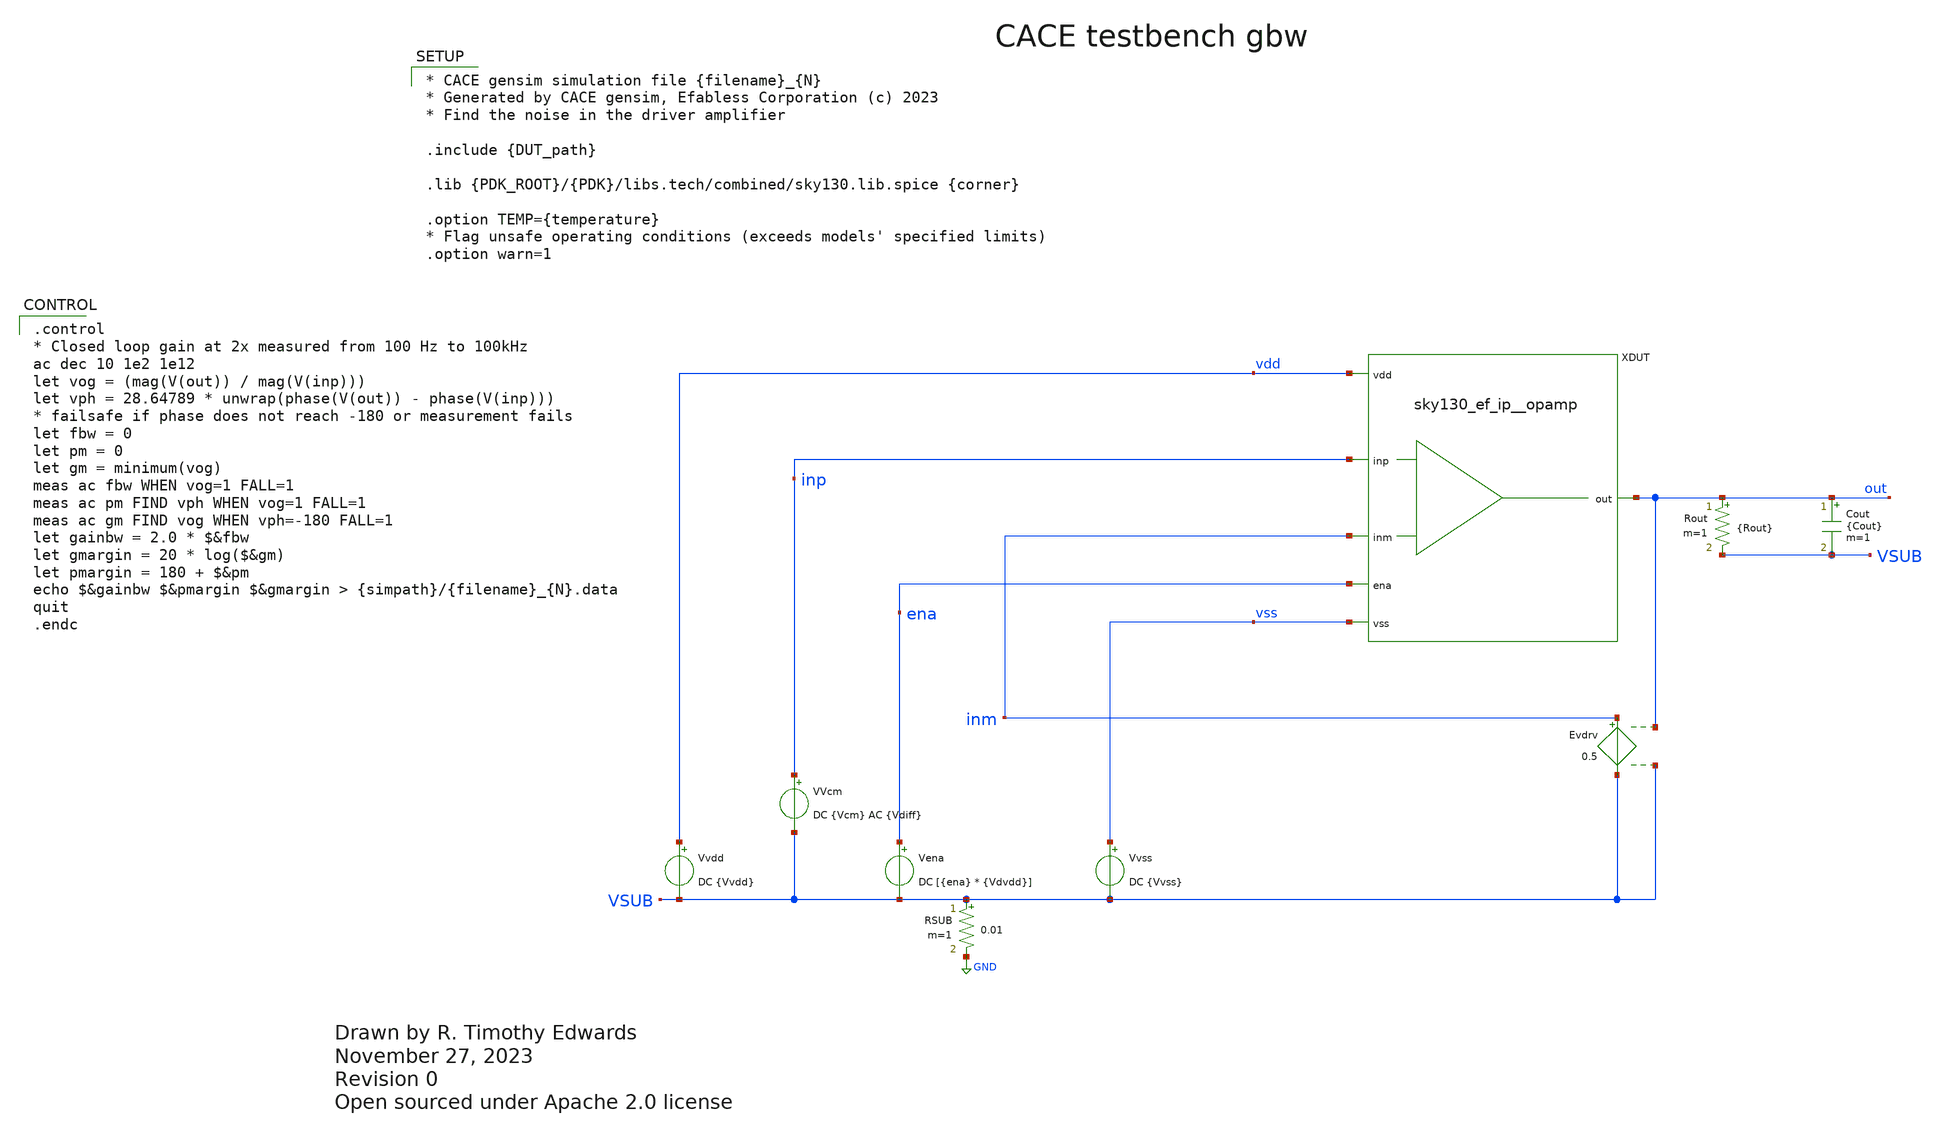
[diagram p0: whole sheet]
** sch_path: cace/templates/gbw.sch
* Open sourced under Apache 2.0 license
**.subckt gbw
VVcm inp VSUB DC {Vcm} AC {Vdiff}
Vena ena VSUB DC [{ena} * {Vdvdd}]
Vvss vss VSUB DC {Vvss}
Rout out VSUB {Rout} m=1
Cout out VSUB {Cout} m=1
Vvdd vdd VSUB DC {Vvdd}
RSUB VSUB GND 0.01 m=1
XDUT vdd out ena vss inp inm sky130_ef_ip__opamp
Evdrv inm VSUB out VSUB 0.5
**** begin user architecture code

.control
* Closed loop gain at 2x measured from 100 Hz to 100kHz
ac dec 10 1e2 1e12
let vog = (mag(V(out)) / mag(V(inp)))
let vph = 28.64789 * unwrap(phase(V(out)) - phase(V(inp)))
* failsafe if phase does not reach -180 or measurement fails
let fbw = 0
let pm = 0
let gm = minimum(vog)
meas ac fbw WHEN vog=1 FALL=1
meas ac pm FIND vph WHEN vog=1 FALL=1
meas ac gm FIND vog WHEN vph=-180 FALL=1
let gainbw = 2.0 * $&fbw
let gmargin = 20 * log($&gm)
let pmargin = 180 + $&pm
echo $&gainbw $&pmargin $&gmargin > {simpath}/{filename}_{N}.data
quit
.endc



* CACE gensim simulation file {filename}_{N}
* Generated by CACE gensim, Efabless Corporation (c) 2023
* Find the noise in the driver amplifier

.include {DUT_path}

.lib {PDK_ROOT}/{PDK}/libs.tech/combined/sky130.lib.spice {corner}

.option TEMP={temperature}
* Flag unsafe operating conditions (exceeds models' specified limits)
.option warn=1


**** end user architecture code
**.ends

* expanding   symbol:  sky130_ef_ip__opamp.sym # of pins=6
** sym_path: xschem/sky130_ef_ip__opamp.sym
** sch_path: xschem/sky130_ef_ip__opamp.sch
.subckt sky130_ef_ip__opamp vdd out ena vss inp inm
*.ipin inp
*.ipin vdd
*.ipin vss
*.opin out
*.ipin ena
*.ipin inm
XM4 pdrv1 net1 vdd vdd sky130_fd_pr__pfet_g5v0d10v5 L=0.5 W=2 nf=2 ad='int((nf+1)/2) * W/nf * 0.29' as='int((nf+2)/2)
+ * W/nf * 0.29' pd='2*int((nf+1)/2) * (W/nf + 0.29)' ps='2*int((nf+2)/2) * (W/nf + 0.29)' nrd='0.29 /
+ W' nrs='0.29 / W' sa=0 sb=0 sd=0 mult=1 m=1
XM5 vdd net1 net1 vdd sky130_fd_pr__pfet_g5v0d10v5 L=0.5 W=2 nf=2 ad='int((nf+1)/2) * W/nf * 0.29' as='int((nf+2)/2)
+ * W/nf * 0.29' pd='2*int((nf+1)/2) * (W/nf + 0.29)' ps='2*int((nf+2)/2) * (W/nf + 0.29)' nrd='0.29 /
+ W' nrs='0.29 / W' sa=0 sb=0 sd=0 mult=1 m=1
XM9 vcomn1 nbias vss vss sky130_fd_pr__nfet_g5v0d10v5 L=0.5 W=1 nf=1 ad='int((nf+1)/2) * W/nf * 0.29' as='int((nf+2)/2)
+ * W/nf * 0.29' pd='2*int((nf+1)/2) * (W/nf + 0.29)' ps='2*int((nf+2)/2) * (W/nf + 0.29)' nrd='0.29 /
+ W' nrs='0.29 / W' sa=0 sb=0 sd=0 mult=1 m=1
XM10 vss nbias nbias vss sky130_fd_pr__nfet_g5v0d10v5 L=0.5 W=4 nf=4 ad='int((nf+1)/2) * W/nf * 0.29' as='int((nf+2)/2)
+ * W/nf * 0.29' pd='2*int((nf+1)/2) * (W/nf + 0.29)' ps='2*int((nf+2)/2) * (W/nf + 0.29)' nrd='0.29 /
+ W' nrs='0.29 / W' sa=0 sb=0 sd=0 mult=1 m=1
XR1 net4 vdd vss sky130_fd_pr__res_xhigh_po_0p35 W=1 L=100 mult=1 m=1
XM20 out pdrv1 vdd vdd sky130_fd_pr__pfet_g5v0d10v5 L=0.5 W=200 nf=200 ad='int((nf+1)/2) * W/nf * 0.29' as='int((nf+2)/2)
+ * W/nf * 0.29' pd='2*int((nf+1)/2) * (W/nf + 0.29)' ps='2*int((nf+2)/2) * (W/nf + 0.29)' nrd='0.29 /
+ W' nrs='0.29 / W' sa=0 sb=0 sd=0 mult=1 m=1
XM22 out ndrv vss vss sky130_fd_pr__nfet_g5v0d10v5 L=0.5 W=120 nf=120 ad='int((nf+1)/2) * W/nf * 0.29' as='int((nf+2)/2)
+ * W/nf * 0.29' pd='2*int((nf+1)/2) * (W/nf + 0.29)' ps='2*int((nf+2)/2) * (W/nf + 0.29)' nrd='0.29 /
+ W' nrs='0.29 / W' sa=0 sb=0 sd=0 mult=1 m=1
XM24 pbias nbias vss vss sky130_fd_pr__nfet_g5v0d10v5 L=0.5 W=1 nf=1 ad='int((nf+1)/2) * W/nf * 0.29' as='int((nf+2)/2)
+ * W/nf * 0.29' pd='2*int((nf+1)/2) * (W/nf + 0.29)' ps='2*int((nf+2)/2) * (W/nf + 0.29)' nrd='0.29 /
+ W' nrs='0.29 / W' sa=0 sb=0 sd=0 mult=1 m=1
XM25 vdd pbias pbias vdd sky130_fd_pr__pfet_g5v0d10v5 L=0.5 W=1 nf=1 ad='int((nf+1)/2) * W/nf * 0.29' as='int((nf+2)/2)
+ * W/nf * 0.29' pd='2*int((nf+1)/2) * (W/nf + 0.29)' ps='2*int((nf+2)/2) * (W/nf + 0.29)' nrd='0.29 /
+ W' nrs='0.29 / W' sa=0 sb=0 sd=0 mult=1 m=1
XM26 vcomp pbias vdd vdd sky130_fd_pr__pfet_g5v0d10v5 L=0.5 W=2 nf=2 ad='int((nf+1)/2) * W/nf * 0.29' as='int((nf+2)/2)
+ * W/nf * 0.29' pd='2*int((nf+1)/2) * (W/nf + 0.29)' ps='2*int((nf+2)/2) * (W/nf + 0.29)' nrd='0.29 /
+ W' nrs='0.29 / W' sa=0 sb=0 sd=0 mult=1 m=1
XM27 net2 inm vcomp vdd sky130_fd_pr__pfet_g5v0d10v5 L=0.5 W=2 nf=2 ad='int((nf+1)/2) * W/nf * 0.29' as='int((nf+2)/2)
+ * W/nf * 0.29' pd='2*int((nf+1)/2) * (W/nf + 0.29)' ps='2*int((nf+2)/2) * (W/nf + 0.29)' nrd='0.29 /
+ W' nrs='0.29 / W' sa=0 sb=0 sd=0 mult=1 m=1
XM28 vcomp inp ndrv vdd sky130_fd_pr__pfet_g5v0d10v5 L=0.5 W=2 nf=2 ad='int((nf+1)/2) * W/nf * 0.29' as='int((nf+2)/2)
+ * W/nf * 0.29' pd='2*int((nf+1)/2) * (W/nf + 0.29)' ps='2*int((nf+2)/2) * (W/nf + 0.29)' nrd='0.29 /
+ W' nrs='0.29 / W' sa=0 sb=0 sd=0 mult=1 m=1
XM29 ndrv net2 vss vss sky130_fd_pr__nfet_g5v0d10v5 L=0.5 W=1 nf=1 ad='int((nf+1)/2) * W/nf * 0.29' as='int((nf+2)/2)
+ * W/nf * 0.29' pd='2*int((nf+1)/2) * (W/nf + 0.29)' ps='2*int((nf+2)/2) * (W/nf + 0.29)' nrd='0.29 /
+ W' nrs='0.29 / W' sa=0 sb=0 sd=0 mult=1 m=1
XM30 vss net2 net2 vss sky130_fd_pr__nfet_g5v0d10v5 L=0.5 W=1 nf=1 ad='int((nf+1)/2) * W/nf * 0.29' as='int((nf+2)/2)
+ * W/nf * 0.29' pd='2*int((nf+1)/2) * (W/nf + 0.29)' ps='2*int((nf+2)/2) * (W/nf + 0.29)' nrd='0.29 /
+ W' nrs='0.29 / W' sa=0 sb=0 sd=0 mult=1 m=1
XM1 net1 inm vcomn1 vss sky130_fd_pr__nfet_g5v0d10v5 L=0.5 W=1 nf=1 ad='int((nf+1)/2) * W/nf * 0.29' as='int((nf+2)/2)
+ * W/nf * 0.29' pd='2*int((nf+1)/2) * (W/nf + 0.29)' ps='2*int((nf+2)/2) * (W/nf + 0.29)' nrd='0.29 /
+ W' nrs='0.29 / W' sa=0 sb=0 sd=0 mult=1 m=1
XM2 vcomn1 inp pdrv1 vss sky130_fd_pr__nfet_g5v0d10v5 L=0.5 W=1 nf=1 ad='int((nf+1)/2) * W/nf * 0.29' as='int((nf+2)/2)
+ * W/nf * 0.29' pd='2*int((nf+1)/2) * (W/nf + 0.29)' ps='2*int((nf+2)/2) * (W/nf + 0.29)' nrd='0.29 /
+ W' nrs='0.29 / W' sa=0 sb=0 sd=0 mult=1 m=1
XM3 pdrv2 net3 vdd vdd sky130_fd_pr__pfet_g5v0d10v5 L=0.5 W=2 nf=2 ad='int((nf+1)/2) * W/nf * 0.29' as='int((nf+2)/2)
+ * W/nf * 0.29' pd='2*int((nf+1)/2) * (W/nf + 0.29)' ps='2*int((nf+2)/2) * (W/nf + 0.29)' nrd='0.29 /
+ W' nrs='0.29 / W' sa=0 sb=0 sd=0 mult=1 m=1
XM6 vdd net3 net3 vdd sky130_fd_pr__pfet_g5v0d10v5 L=0.5 W=2 nf=2 ad='int((nf+1)/2) * W/nf * 0.29' as='int((nf+2)/2)
+ * W/nf * 0.29' pd='2*int((nf+1)/2) * (W/nf + 0.29)' ps='2*int((nf+2)/2) * (W/nf + 0.29)' nrd='0.29 /
+ W' nrs='0.29 / W' sa=0 sb=0 sd=0 mult=1 m=1
XM7 vcomn2 nbias vss vss sky130_fd_pr__nfet_g5v0d10v5 L=0.5 W=1 nf=1 ad='int((nf+1)/2) * W/nf * 0.29' as='int((nf+2)/2)
+ * W/nf * 0.29' pd='2*int((nf+1)/2) * (W/nf + 0.29)' ps='2*int((nf+2)/2) * (W/nf + 0.29)' nrd='0.29 /
+ W' nrs='0.29 / W' sa=0 sb=0 sd=0 mult=1 m=1
XM8 net3 inm vcomn2 vss sky130_fd_pr__nfet_03v3_nvt L=0.5 W=1 nf=1 ad='int((nf+1)/2) * W/nf * 0.29' as='int((nf+2)/2)
+ * W/nf * 0.29' pd='2*int((nf+1)/2) * (W/nf + 0.29)' ps='2*int((nf+2)/2) * (W/nf + 0.29)' nrd='0.29 /
+ W' nrs='0.29 / W' sa=0 sb=0 sd=0 mult=1 m=1
XM11 vcomn2 inp pdrv2 vss sky130_fd_pr__nfet_03v3_nvt L=0.5 W=1 nf=1 ad='int((nf+1)/2) * W/nf * 0.29' as='int((nf+2)/2)
+ * W/nf * 0.29' pd='2*int((nf+1)/2) * (W/nf + 0.29)' ps='2*int((nf+2)/2) * (W/nf + 0.29)' nrd='0.29 /
+ W' nrs='0.29 / W' sa=0 sb=0 sd=0 mult=1 m=1
XM12 vdd pdrv2 out vdd sky130_fd_pr__pfet_g5v0d10v5 L=0.5 W=200 nf=200 ad='int((nf+1)/2) * W/nf * 0.29' as='int((nf+2)/2)
+ * W/nf * 0.29' pd='2*int((nf+1)/2) * (W/nf + 0.29)' ps='2*int((nf+2)/2) * (W/nf + 0.29)' nrd='0.29 /
+ W' nrs='0.29 / W' sa=0 sb=0 sd=0 mult=1 m=1
XXD1 vss inp sky130_fd_pr__diode_pw2nd_05v5 area=3.6e11 pj=4e6
XM13 net4 ena nbias vss sky130_fd_pr__nfet_g5v0d10v5 L=0.5 W=1 nf=1 ad='int((nf+1)/2) * W/nf * 0.29' as='int((nf+2)/2)
+ * W/nf * 0.29' pd='2*int((nf+1)/2) * (W/nf + 0.29)' ps='2*int((nf+2)/2) * (W/nf + 0.29)' nrd='0.29 /
+ W' nrs='0.29 / W' sa=0 sb=0 sd=0 mult=1 m=1
XXD2 vss ena sky130_fd_pr__diode_pw2nd_05v5 area=3.6e11 pj=4e6
XXD3 vss inm sky130_fd_pr__diode_pw2nd_05v5 area=3.6e11 pj=4e6
.ends

.GLOBAL GND
.end
